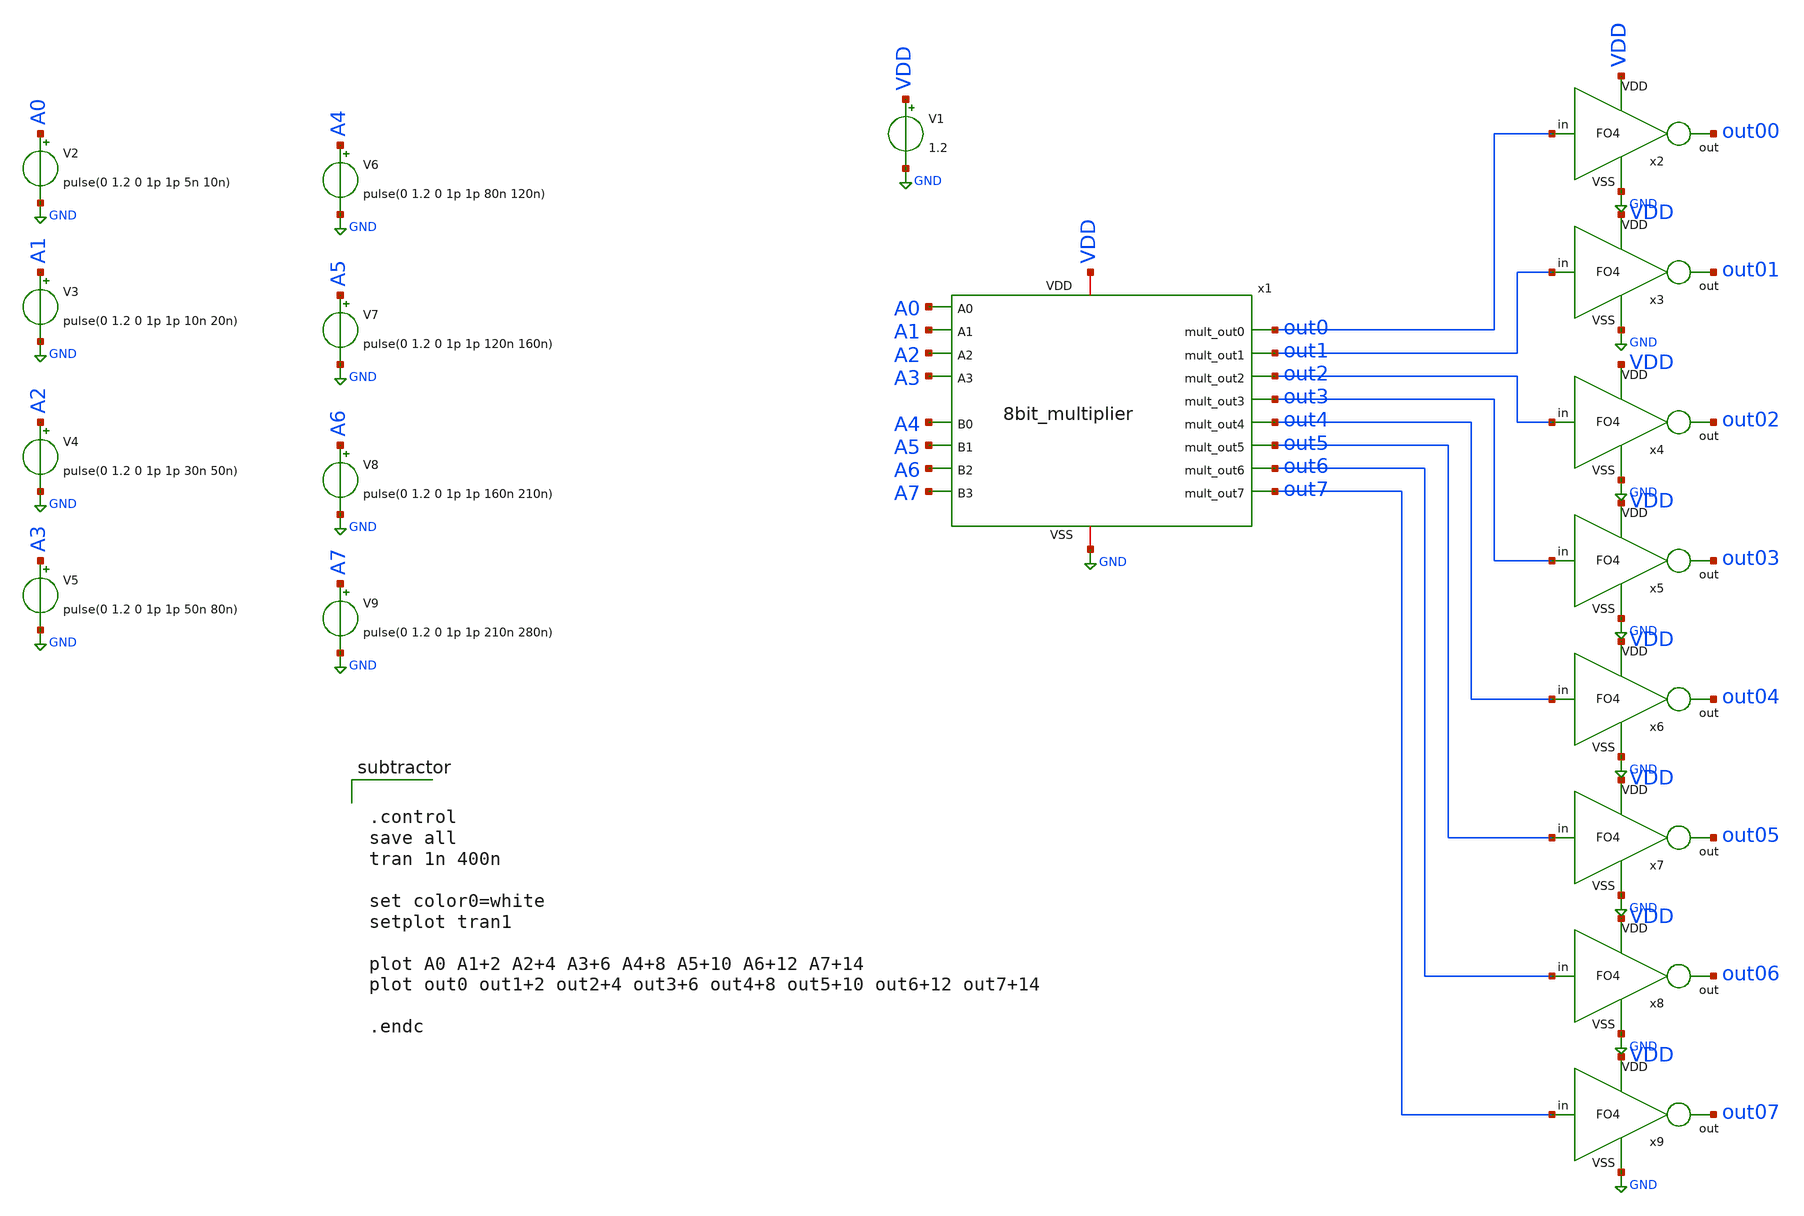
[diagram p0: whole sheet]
** sch_path: multiplier_tb.sch
**.subckt multiplier_tb
V1 VDD GND 1.2
V2 A0 GND pulse(0 1.2 0 1p 1p 5n 10n)
V3 A1 GND pulse(0 1.2 0 1p 1p 10n 20n)
V4 A2 GND pulse(0 1.2 0 1p 1p 30n 50n)
V5 A3 GND pulse(0 1.2 0 1p 1p 50n 80n)
V6 A4 GND pulse(0 1.2 0 1p 1p 80n 120n)
V7 A5 GND pulse(0 1.2 0 1p 1p 120n 160n)
V8 A6 GND pulse(0 1.2 0 1p 1p 160n 210n)
V9 A7 GND pulse(0 1.2 0 1p 1p 210n 280n)
x2 VDD GND out0 out00 FO4
x3 VDD GND out1 out01 FO4
x4 VDD GND out2 out02 FO4
x5 VDD GND out3 out03 FO4
x6 VDD GND out4 out04 FO4
x7 VDD GND out5 out05 FO4
x8 VDD GND out6 out06 FO4
x9 VDD GND out7 out07 FO4
x1 VDD GND A0 out1 A1 out2 out0 A6 out3 out4 out7 out6 out5 A2 A7 A3 A5 A4 8bit_multiplier
**** begin user architecture code

** opencircuitdesign pdks install
.lib $::SKYWATER_MODELS/sky130.lib.spice tt_mm




.control
save all
tran 1n 400n

set color0=white
setplot tran1

plot A0 A1+2 A2+4 A3+6 A4+8 A5+10 A6+12 A7+14
plot out0 out1+2 out2+4 out3+6 out4+8 out5+10 out6+12 out7+14

.endc


**** end user architecture code
**.ends
.GLOBAL GND
.end
